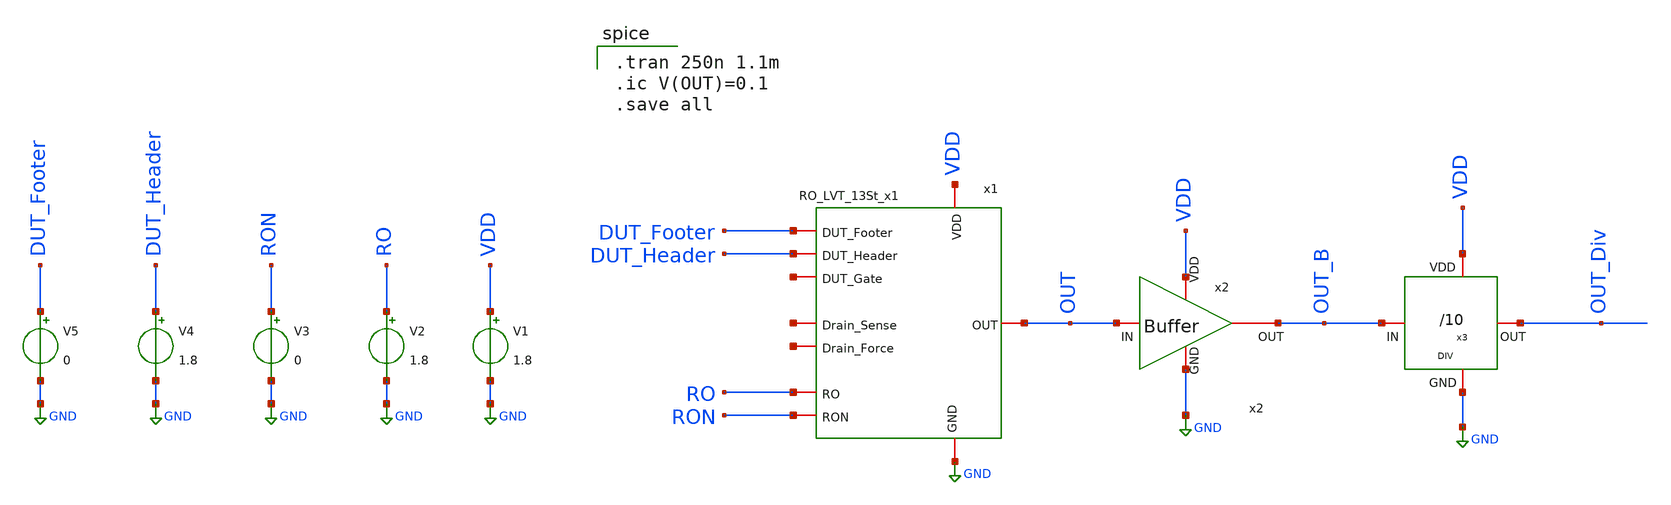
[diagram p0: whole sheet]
** sch_path: TB/13St_TB.sch
**.subckt 13St_TB
V1 VDD GND 1.8
V2 RO GND 1.8
V3 RON GND 0
V4 DUT_Header GND 1.8
V5 DUT_Footer GND 0
x2 VDD OUT OUT_B GND Buffer
x1 VDD GND DUT_Footer DUT_Header net1 net2 RO RON net3 OUT RO_LVT_13St_x1
x3 VDD OUT_Div OUT_B GND DIV
**** begin user architecture code

.tran 250n 1.1m
.ic V(OUT)=0.1
.save all

 .lib $::SKYWATER_MODELS/sky130.lib.spice tt
.include $::SKYWATER_STDCELLS/sky130_fd_sc_hd.spice

**** end user architecture code
**.ends
.GLOBAL GND
.GLOBAL VDD
.end
